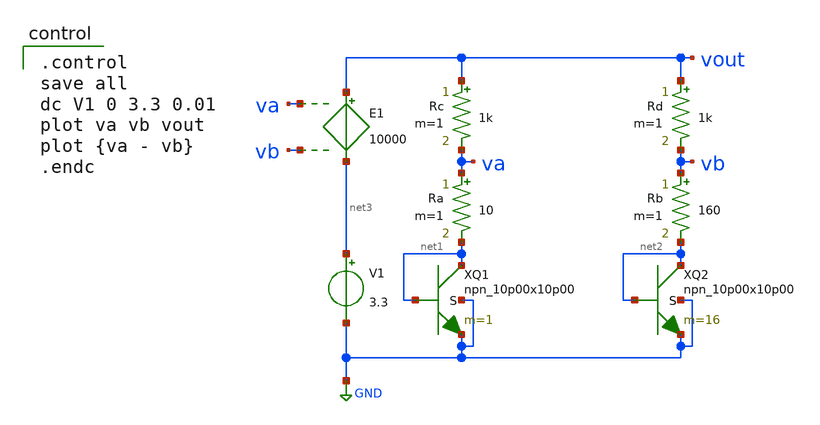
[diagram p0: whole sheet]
** sch_path: bgr/npn-diode-vcvs.sch
**.subckt npn-diode-vcvs
XQ1 net1 net1 GND GND npn_10p00x10p00 m=1
XQ2 net2 net2 GND GND npn_10p00x10p00 m=16
Rb vb net2 160 m=1
Ra va net1 10 m=1
Rc vout va 1k m=1
Rd vout vb 1k m=1
E1 vout net3 va vb 10000
V1 net3 GND 3.3
**** begin user architecture code

.include $::180MCU_MODELS/design.ngspice
.lib $::180MCU_MODELS/sm141064.ngspice typical
.lib $::180MCU_MODELS/sm141064.ngspice res_typical
.lib $::180MCU_MODELS/sm141064.ngspice moscap_typical
.lib $::180MCU_MODELS/sm141064.ngspice bjt_typical
* .lib $::180MCU_MODELS/sm141064.ngspice res_statistical


.control
save all
dc V1 0 3.3 0.01
plot va vb vout
plot {va - vb}
.endc

**** end user architecture code
**.ends
.GLOBAL GND
.end
